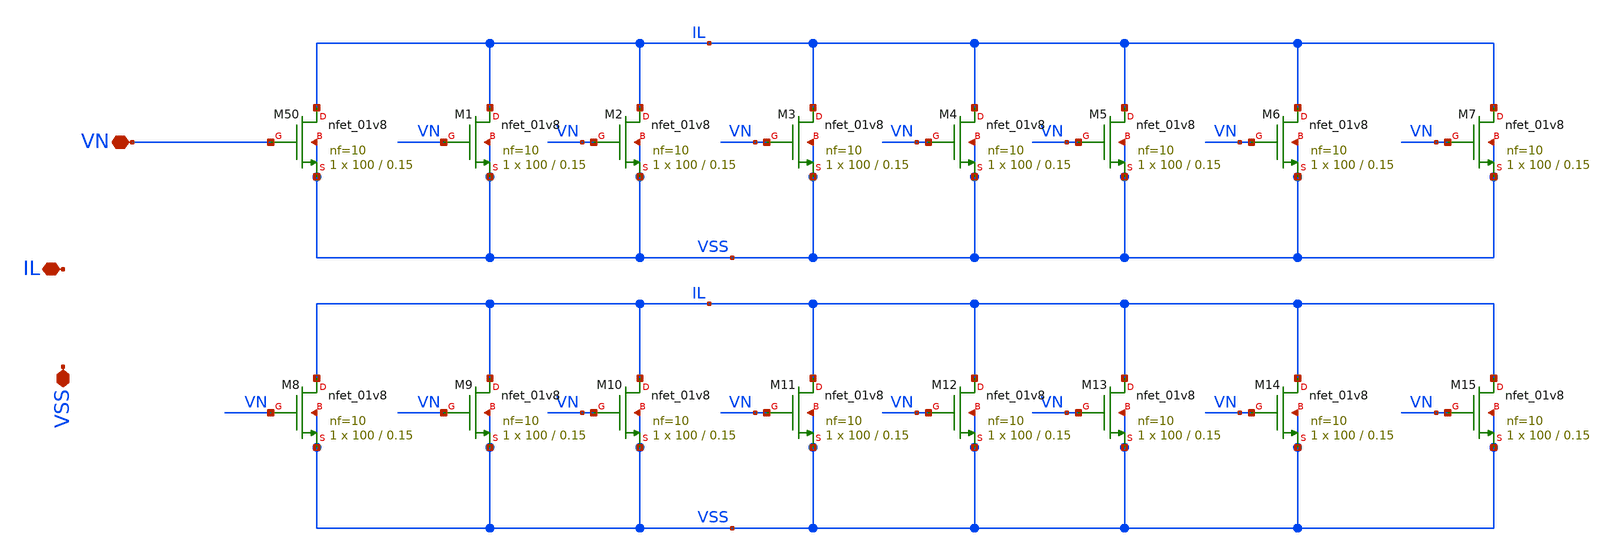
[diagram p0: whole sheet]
** sch_path: xschem/DC_DC_Converter_xschem/DC_DC_Converter/Power_Mosfet/N_Power_mosfets.sch
**.subckt N_Power_mosfets VSS VN IL
*.iopin VSS
*.iopin VN
*.iopin IL
XM50 IL VN VSS VSS sky130_fd_pr__nfet_01v8 L=0.15 W=100 nf=10 ad='int((nf+1)/2) * W/nf * 0.29' as='int((nf+2)/2) * W/nf * 0.29'
+ pd='2*int((nf+1)/2) * (W/nf + 0.29)' ps='2*int((nf+2)/2) * (W/nf + 0.29)' nrd='0.29 / W' nrs='0.29 / W'
+ sa=0 sb=0 sd=0 mult=1 m=1
XM1 IL VN VSS VSS sky130_fd_pr__nfet_01v8 L=0.15 W=100 nf=10 ad='int((nf+1)/2) * W/nf * 0.29' as='int((nf+2)/2) * W/nf * 0.29'
+ pd='2*int((nf+1)/2) * (W/nf + 0.29)' ps='2*int((nf+2)/2) * (W/nf + 0.29)' nrd='0.29 / W' nrs='0.29 / W'
+ sa=0 sb=0 sd=0 mult=1 m=1
XM2 IL VN VSS VSS sky130_fd_pr__nfet_01v8 L=0.15 W=100 nf=10 ad='int((nf+1)/2) * W/nf * 0.29' as='int((nf+2)/2) * W/nf * 0.29'
+ pd='2*int((nf+1)/2) * (W/nf + 0.29)' ps='2*int((nf+2)/2) * (W/nf + 0.29)' nrd='0.29 / W' nrs='0.29 / W'
+ sa=0 sb=0 sd=0 mult=1 m=1
XM3 IL VN VSS VSS sky130_fd_pr__nfet_01v8 L=0.15 W=100 nf=10 ad='int((nf+1)/2) * W/nf * 0.29' as='int((nf+2)/2) * W/nf * 0.29'
+ pd='2*int((nf+1)/2) * (W/nf + 0.29)' ps='2*int((nf+2)/2) * (W/nf + 0.29)' nrd='0.29 / W' nrs='0.29 / W'
+ sa=0 sb=0 sd=0 mult=1 m=1
XM4 IL VN VSS VSS sky130_fd_pr__nfet_01v8 L=0.15 W=100 nf=10 ad='int((nf+1)/2) * W/nf * 0.29' as='int((nf+2)/2) * W/nf * 0.29'
+ pd='2*int((nf+1)/2) * (W/nf + 0.29)' ps='2*int((nf+2)/2) * (W/nf + 0.29)' nrd='0.29 / W' nrs='0.29 / W'
+ sa=0 sb=0 sd=0 mult=1 m=1
XM5 IL VN VSS VSS sky130_fd_pr__nfet_01v8 L=0.15 W=100 nf=10 ad='int((nf+1)/2) * W/nf * 0.29' as='int((nf+2)/2) * W/nf * 0.29'
+ pd='2*int((nf+1)/2) * (W/nf + 0.29)' ps='2*int((nf+2)/2) * (W/nf + 0.29)' nrd='0.29 / W' nrs='0.29 / W'
+ sa=0 sb=0 sd=0 mult=1 m=1
XM6 IL VN VSS VSS sky130_fd_pr__nfet_01v8 L=0.15 W=100 nf=10 ad='int((nf+1)/2) * W/nf * 0.29' as='int((nf+2)/2) * W/nf * 0.29'
+ pd='2*int((nf+1)/2) * (W/nf + 0.29)' ps='2*int((nf+2)/2) * (W/nf + 0.29)' nrd='0.29 / W' nrs='0.29 / W'
+ sa=0 sb=0 sd=0 mult=1 m=1
XM7 IL VN VSS VSS sky130_fd_pr__nfet_01v8 L=0.15 W=100 nf=10 ad='int((nf+1)/2) * W/nf * 0.29' as='int((nf+2)/2) * W/nf * 0.29'
+ pd='2*int((nf+1)/2) * (W/nf + 0.29)' ps='2*int((nf+2)/2) * (W/nf + 0.29)' nrd='0.29 / W' nrs='0.29 / W'
+ sa=0 sb=0 sd=0 mult=1 m=1
XM8 IL VN VSS VSS sky130_fd_pr__nfet_01v8 L=0.15 W=100 nf=10 ad='int((nf+1)/2) * W/nf * 0.29' as='int((nf+2)/2) * W/nf * 0.29'
+ pd='2*int((nf+1)/2) * (W/nf + 0.29)' ps='2*int((nf+2)/2) * (W/nf + 0.29)' nrd='0.29 / W' nrs='0.29 / W'
+ sa=0 sb=0 sd=0 mult=1 m=1
XM9 IL VN VSS VSS sky130_fd_pr__nfet_01v8 L=0.15 W=100 nf=10 ad='int((nf+1)/2) * W/nf * 0.29' as='int((nf+2)/2) * W/nf * 0.29'
+ pd='2*int((nf+1)/2) * (W/nf + 0.29)' ps='2*int((nf+2)/2) * (W/nf + 0.29)' nrd='0.29 / W' nrs='0.29 / W'
+ sa=0 sb=0 sd=0 mult=1 m=1
XM10 IL VN VSS VSS sky130_fd_pr__nfet_01v8 L=0.15 W=100 nf=10 ad='int((nf+1)/2) * W/nf * 0.29' as='int((nf+2)/2) * W/nf * 0.29'
+ pd='2*int((nf+1)/2) * (W/nf + 0.29)' ps='2*int((nf+2)/2) * (W/nf + 0.29)' nrd='0.29 / W' nrs='0.29 / W'
+ sa=0 sb=0 sd=0 mult=1 m=1
XM11 IL VN VSS VSS sky130_fd_pr__nfet_01v8 L=0.15 W=100 nf=10 ad='int((nf+1)/2) * W/nf * 0.29' as='int((nf+2)/2) * W/nf * 0.29'
+ pd='2*int((nf+1)/2) * (W/nf + 0.29)' ps='2*int((nf+2)/2) * (W/nf + 0.29)' nrd='0.29 / W' nrs='0.29 / W'
+ sa=0 sb=0 sd=0 mult=1 m=1
XM12 IL VN VSS VSS sky130_fd_pr__nfet_01v8 L=0.15 W=100 nf=10 ad='int((nf+1)/2) * W/nf * 0.29' as='int((nf+2)/2) * W/nf * 0.29'
+ pd='2*int((nf+1)/2) * (W/nf + 0.29)' ps='2*int((nf+2)/2) * (W/nf + 0.29)' nrd='0.29 / W' nrs='0.29 / W'
+ sa=0 sb=0 sd=0 mult=1 m=1
XM13 IL VN VSS VSS sky130_fd_pr__nfet_01v8 L=0.15 W=100 nf=10 ad='int((nf+1)/2) * W/nf * 0.29' as='int((nf+2)/2) * W/nf * 0.29'
+ pd='2*int((nf+1)/2) * (W/nf + 0.29)' ps='2*int((nf+2)/2) * (W/nf + 0.29)' nrd='0.29 / W' nrs='0.29 / W'
+ sa=0 sb=0 sd=0 mult=1 m=1
XM14 IL VN VSS VSS sky130_fd_pr__nfet_01v8 L=0.15 W=100 nf=10 ad='int((nf+1)/2) * W/nf * 0.29' as='int((nf+2)/2) * W/nf * 0.29'
+ pd='2*int((nf+1)/2) * (W/nf + 0.29)' ps='2*int((nf+2)/2) * (W/nf + 0.29)' nrd='0.29 / W' nrs='0.29 / W'
+ sa=0 sb=0 sd=0 mult=1 m=1
XM15 IL VN VSS VSS sky130_fd_pr__nfet_01v8 L=0.15 W=100 nf=10 ad='int((nf+1)/2) * W/nf * 0.29' as='int((nf+2)/2) * W/nf * 0.29'
+ pd='2*int((nf+1)/2) * (W/nf + 0.29)' ps='2*int((nf+2)/2) * (W/nf + 0.29)' nrd='0.29 / W' nrs='0.29 / W'
+ sa=0 sb=0 sd=0 mult=1 m=1
**.ends
.end
